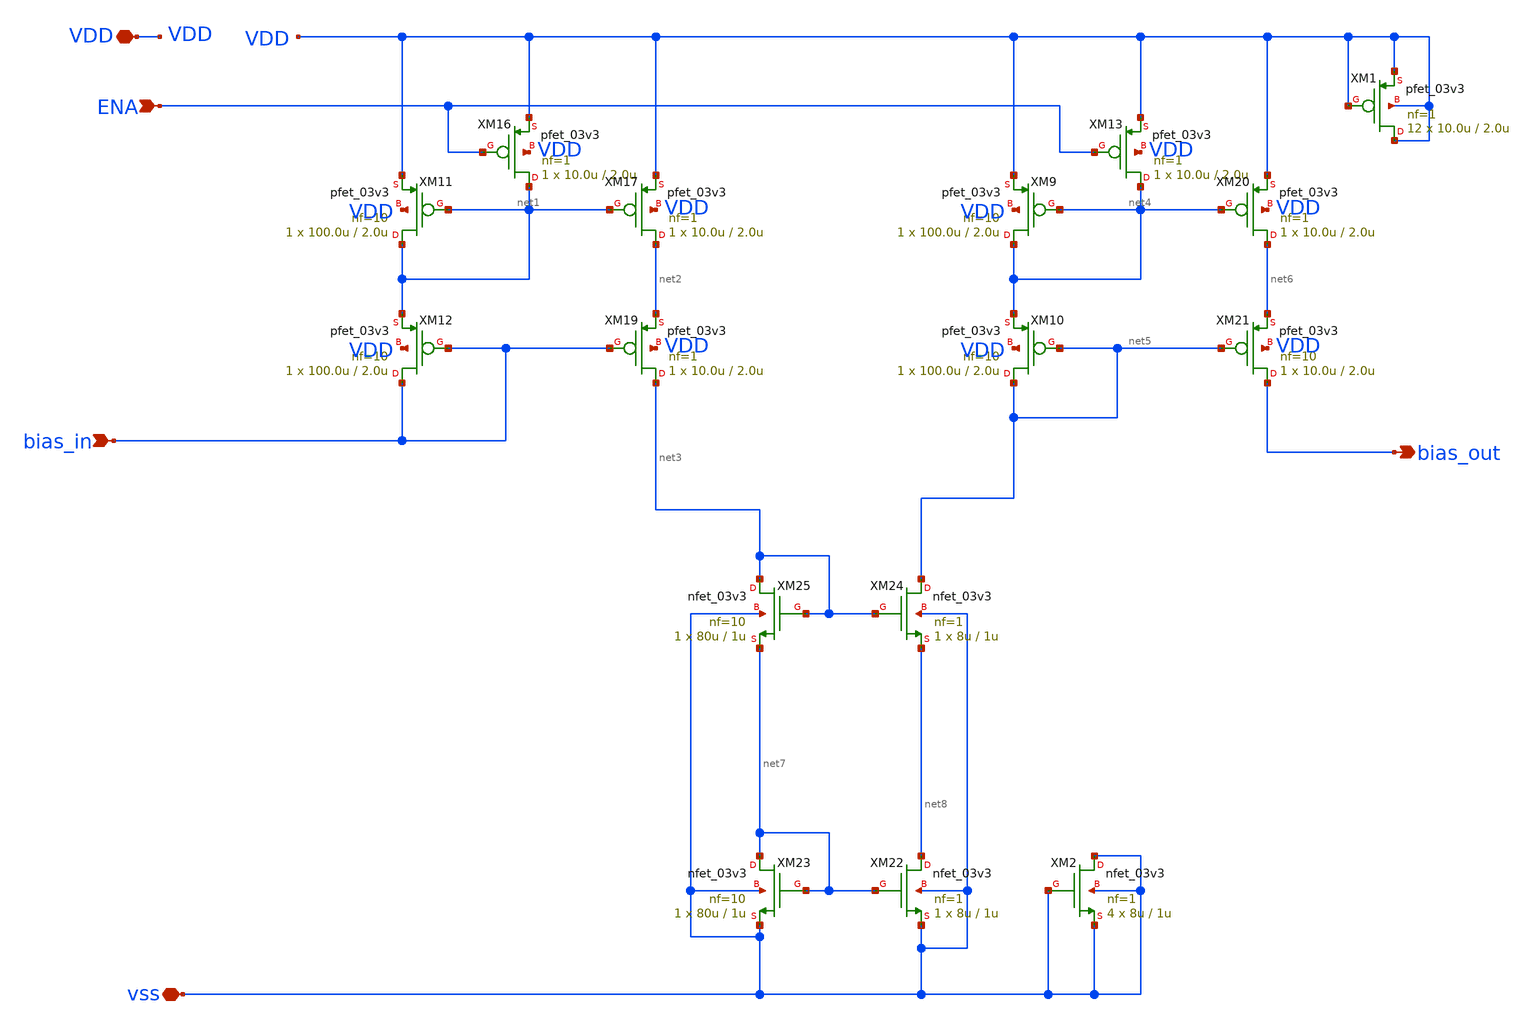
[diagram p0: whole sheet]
** sch_path: blocks/composite/regulated_cascoded_cmirror/A3_core/bias/bias.sch
**.subckt bias vss VDD ENA bias_in bias_out
*.iopin vss
*.iopin VDD
*.ipin ENA
*.ipin bias_in
*.opin bias_out
XM11 net1 net1 VDD VDD pfet_03v3 L=2.0u W=100.0u nf=10 ad='int((nf+1)/2) * W/nf * 0.18u' as='int((nf+2)/2) * W/nf * 0.18u'
+ pd='2*int((nf+1)/2) * (W/nf + 0.18u)' ps='2*int((nf+2)/2) * (W/nf + 0.18u)' nrd='0.18u / W' nrs='0.18u / W'
+ sa=0 sb=0 sd=0 m=1
XM12 bias_in bias_in net1 VDD pfet_03v3 L=2.0u W=100.0u nf=10 ad='int((nf+1)/2) * W/nf * 0.18u' as='int((nf+2)/2) * W/nf * 0.18u'
+ pd='2*int((nf+1)/2) * (W/nf + 0.18u)' ps='2*int((nf+2)/2) * (W/nf + 0.18u)' nrd='0.18u / W' nrs='0.18u / W'
+ sa=0 sb=0 sd=0 m=1
XM16 net1 ENA VDD VDD pfet_03v3 L=2.0u W=10.0u nf=1 ad='int((nf+1)/2) * W/nf * 0.18u' as='int((nf+2)/2) * W/nf * 0.18u'
+ pd='2*int((nf+1)/2) * (W/nf + 0.18u)' ps='2*int((nf+2)/2) * (W/nf + 0.18u)' nrd='0.18u / W' nrs='0.18u / W'
+ sa=0 sb=0 sd=0 m=1
XM17 net2 net1 VDD VDD pfet_03v3 L=2.0u W=10.0u nf=1 ad='int((nf+1)/2) * W/nf * 0.18u' as='int((nf+2)/2) * W/nf * 0.18u'
+ pd='2*int((nf+1)/2) * (W/nf + 0.18u)' ps='2*int((nf+2)/2) * (W/nf + 0.18u)' nrd='0.18u / W' nrs='0.18u / W'
+ sa=0 sb=0 sd=0 m=1
XM19 net3 bias_in net2 VDD pfet_03v3 L=2.0u W=10.0u nf=1 ad='int((nf+1)/2) * W/nf * 0.18u' as='int((nf+2)/2) * W/nf * 0.18u'
+ pd='2*int((nf+1)/2) * (W/nf + 0.18u)' ps='2*int((nf+2)/2) * (W/nf + 0.18u)' nrd='0.18u / W' nrs='0.18u / W'
+ sa=0 sb=0 sd=0 m=1
XM9 net4 net4 VDD VDD pfet_03v3 L=2.0u W=100.0u nf=10 ad='int((nf+1)/2) * W/nf * 0.18u' as='int((nf+2)/2) * W/nf * 0.18u'
+ pd='2*int((nf+1)/2) * (W/nf + 0.18u)' ps='2*int((nf+2)/2) * (W/nf + 0.18u)' nrd='0.18u / W' nrs='0.18u / W'
+ sa=0 sb=0 sd=0 m=1
XM10 net5 net5 net4 VDD pfet_03v3 L=2.0u W=100.0u nf=10 ad='int((nf+1)/2) * W/nf * 0.18u' as='int((nf+2)/2) * W/nf * 0.18u'
+ pd='2*int((nf+1)/2) * (W/nf + 0.18u)' ps='2*int((nf+2)/2) * (W/nf + 0.18u)' nrd='0.18u / W' nrs='0.18u / W'
+ sa=0 sb=0 sd=0 m=1
XM13 net4 ENA VDD VDD pfet_03v3 L=2.0u W=10.0u nf=1 ad='int((nf+1)/2) * W/nf * 0.18u' as='int((nf+2)/2) * W/nf * 0.18u'
+ pd='2*int((nf+1)/2) * (W/nf + 0.18u)' ps='2*int((nf+2)/2) * (W/nf + 0.18u)' nrd='0.18u / W' nrs='0.18u / W'
+ sa=0 sb=0 sd=0 m=1
XM20 net6 net4 VDD VDD pfet_03v3 L=2.0u W=10.0u nf=1 ad='int((nf+1)/2) * W/nf * 0.18u' as='int((nf+2)/2) * W/nf * 0.18u'
+ pd='2*int((nf+1)/2) * (W/nf + 0.18u)' ps='2*int((nf+2)/2) * (W/nf + 0.18u)' nrd='0.18u / W' nrs='0.18u / W'
+ sa=0 sb=0 sd=0 m=1
XM21 bias_out net5 net6 VDD pfet_03v3 L=2.0u W=10.0u nf=10 ad='int((nf+1)/2) * W/nf * 0.18u' as='int((nf+2)/2) * W/nf * 0.18u'
+ pd='2*int((nf+1)/2) * (W/nf + 0.18u)' ps='2*int((nf+2)/2) * (W/nf + 0.18u)' nrd='0.18u / W' nrs='0.18u / W'
+ sa=0 sb=0 sd=0 m=1
XM22 net8 net7 vss vss nfet_03v3 L=1u W=8u nf=1 ad='int((nf+1)/2) * W/nf * 0.18u' as='int((nf+2)/2) * W/nf * 0.18u'
+ pd='2*int((nf+1)/2) * (W/nf + 0.18u)' ps='2*int((nf+2)/2) * (W/nf + 0.18u)' nrd='0.18u / W' nrs='0.18u / W'
+ sa=0 sb=0 sd=0 m=1
XM23 net7 net7 vss vss nfet_03v3 L=1u W=80u nf=10 ad='int((nf+1)/2) * W/nf * 0.18u' as='int((nf+2)/2) * W/nf * 0.18u'
+ pd='2*int((nf+1)/2) * (W/nf + 0.18u)' ps='2*int((nf+2)/2) * (W/nf + 0.18u)' nrd='0.18u / W' nrs='0.18u / W'
+ sa=0 sb=0 sd=0 m=1
XM24 net5 net3 net8 vss nfet_03v3 L=1u W=8u nf=1 ad='int((nf+1)/2) * W/nf * 0.18u' as='int((nf+2)/2) * W/nf * 0.18u'
+ pd='2*int((nf+1)/2) * (W/nf + 0.18u)' ps='2*int((nf+2)/2) * (W/nf + 0.18u)' nrd='0.18u / W' nrs='0.18u / W'
+ sa=0 sb=0 sd=0 m=1
XM25 net3 net3 net7 vss nfet_03v3 L=1u W=80u nf=10 ad='int((nf+1)/2) * W/nf * 0.18u' as='int((nf+2)/2) * W/nf * 0.18u'
+ pd='2*int((nf+1)/2) * (W/nf + 0.18u)' ps='2*int((nf+2)/2) * (W/nf + 0.18u)' nrd='0.18u / W' nrs='0.18u / W'
+ sa=0 sb=0 sd=0 m=1
XM1 VDD VDD VDD VDD pfet_03v3 L=2.0u W=10.0u nf=1 ad='int((nf+1)/2) * W/nf * 0.18u' as='int((nf+2)/2) * W/nf * 0.18u'
+ pd='2*int((nf+1)/2) * (W/nf + 0.18u)' ps='2*int((nf+2)/2) * (W/nf + 0.18u)' nrd='0.18u / W' nrs='0.18u / W'
+ sa=0 sb=0 sd=0 m=12
XM2 vss vss vss vss nfet_03v3 L=1u W=8u nf=1 ad='int((nf+1)/2) * W/nf * 0.18u' as='int((nf+2)/2) * W/nf * 0.18u'
+ pd='2*int((nf+1)/2) * (W/nf + 0.18u)' ps='2*int((nf+2)/2) * (W/nf + 0.18u)' nrd='0.18u / W' nrs='0.18u / W'
+ sa=0 sb=0 sd=0 m=4
**.ends
.end
